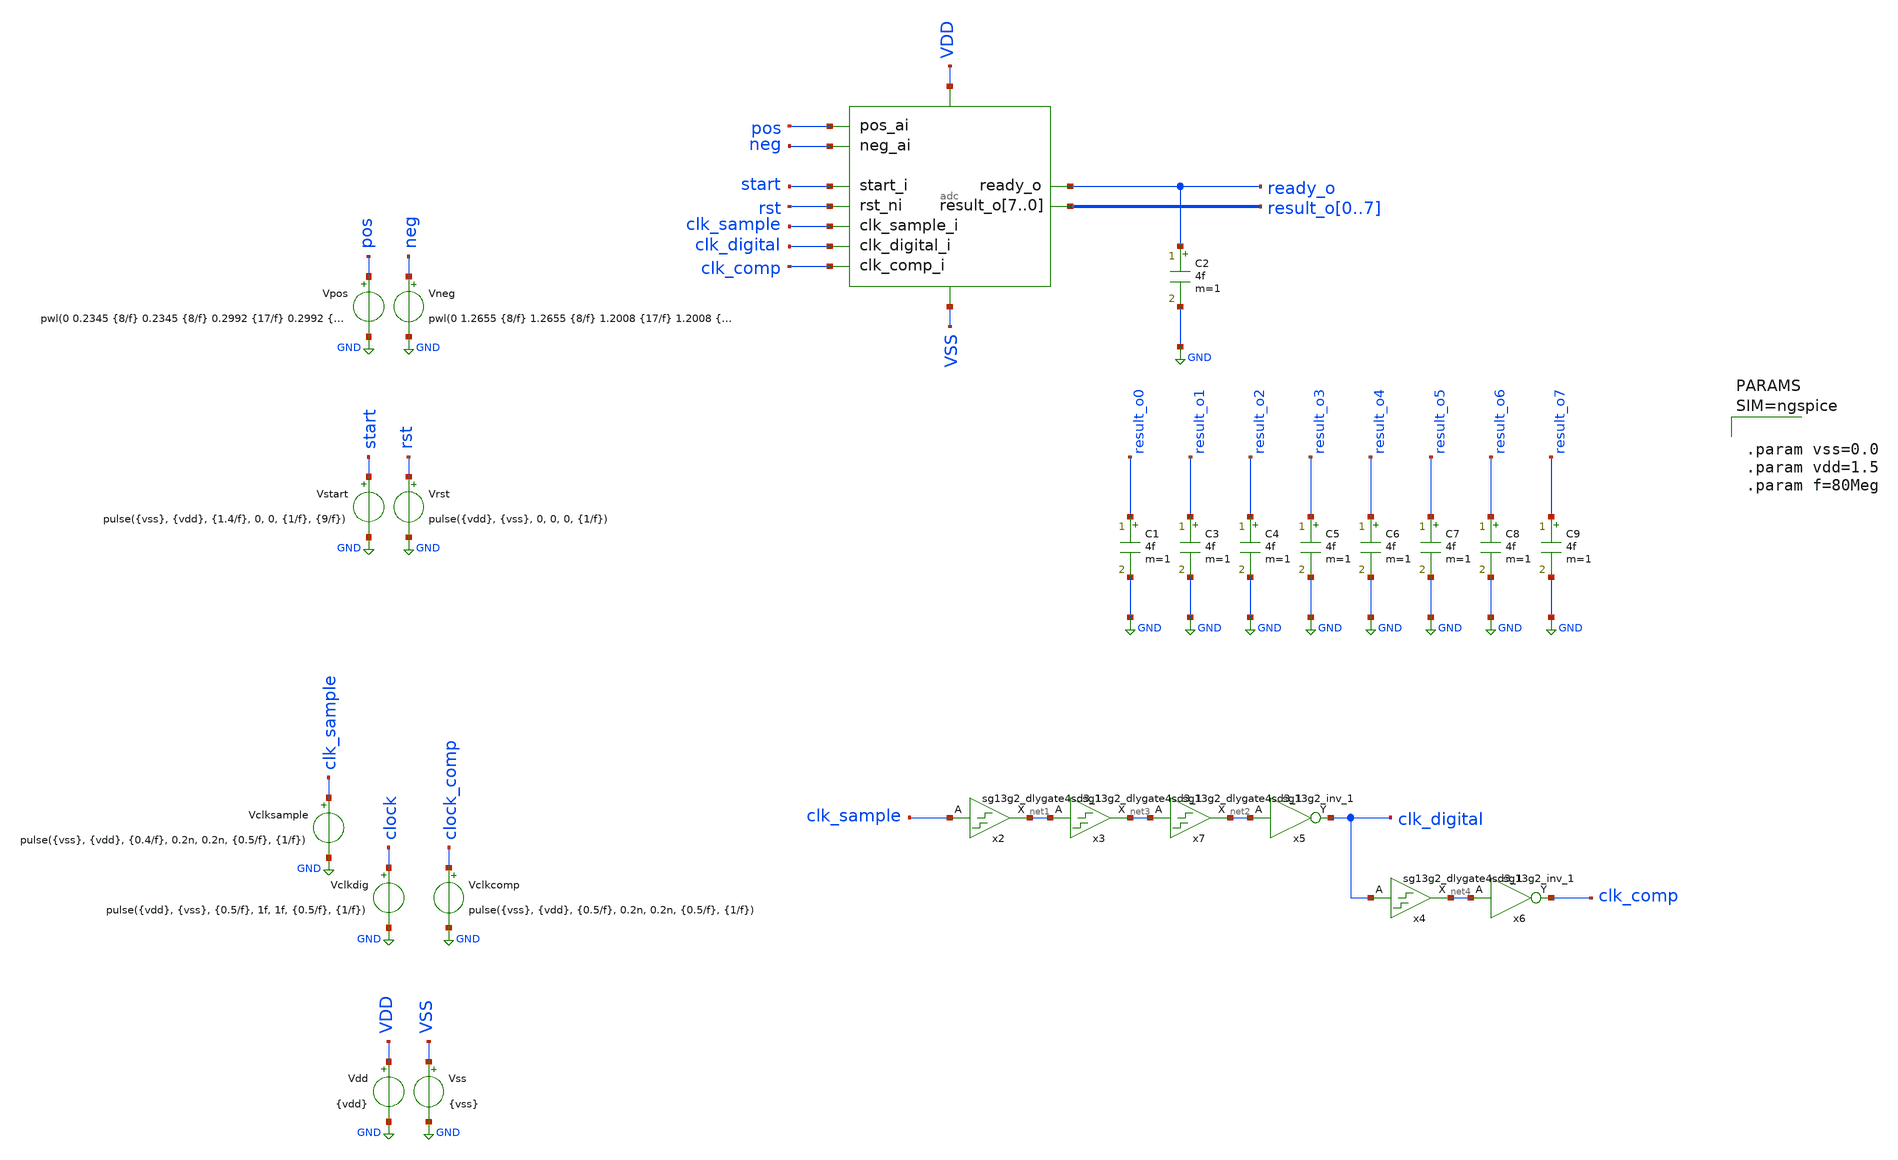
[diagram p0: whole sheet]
** sch_path: project/xschem/adc_tb.sch
* IHP-GmbH/IHP-Open-PDK/ihp-sg13g2/libs.tech/xschem/sg13g2_stdcells/sg13g2_inv_2.sch:
* Copyright 2023 IHP PDK Authors
* Licensed under the Apache License, Version 2.0 (the "License");
**.subckt adc_tb
x1 pos start rst clk_digital result_o0 result_o1 result_o2 result_o3 result_o4 result_o5 result_o6
+ result_o7 ready_o VDD VSS clk_comp neg clk_sample adc
Vclkdig clock GND pulse({vdd}, {vss}, {0.5/f}, 1f, 1f, {0.5/f}, {1/f})
Vrst rst GND pulse({vdd}, {vss}, 0, 0, 0, {1/f})
Vstart start GND pulse({vss}, {vdd}, {1.4/f}, 0, 0, {1/f}, {9/f})
Vpos pos GND pwl(0 0.2345 {8/f} 0.2345 {8/f} 0.2992 {17/f} 0.2992 {17/f} 0.3639 {26/f} 0.3639 {26/f}
+ 0.4286 {35/f} 0.4286 {35/f} 0.4933 {44/f} 0.4933 {44/f} 0.5580 {53/f} 0.5580 {53/f} 0.6227 {62/f} 0.6227
+ {62/f} 0.6875 {71/f} 0.6875 {71/f} 0.7522 {80/f} 0.7522 {80/f} 0.8169 {89/f} 0.8169 {89/f} 0.8816 {98/f}
+ 0.8816 {98/f} 0.9463 {107/f} 0.9463 {107/f} 1.0110 {116/f} 1.0110 {116/f} 1.0757 {125/f} 1.0757 {125/f}
+ 1.1404 {134/f} 1.1404 {134/f} 1.2051 {143/f} 1.2051 {143/f} 1.2698 {152/f} 1.2698)
.save i(vpos)
Vdd VDD GND {vdd}
Vss VSS GND {vss}
C1 result_o0 GND 4f m=1
C2 ready_o GND 4f m=1
C3 result_o1 GND 4f m=1
C4 result_o2 GND 4f m=1
C5 result_o3 GND 4f m=1
Vclkcomp clock_comp GND pulse({vss}, {vdd}, {0.5/f}, 0.2n, 0.2n, {0.5/f}, {1/f})
C6 result_o4 GND 4f m=1
C7 result_o5 GND 4f m=1
C8 result_o6 GND 4f m=1
C9 result_o7 GND 4f m=1
Vneg neg GND pwl(0 1.2655 {8/f} 1.2655 {8/f} 1.2008 {17/f} 1.2008 {17/f} 1.1361 {26/f} 1.1361 {26/f}
+ 1.0714 {35/f} 1.0714 {35/f} 1.0067 {44/f} 1.0067 {44/f} 0.9420 {53/f} 0.9420 {53/f} 0.8773 {62/f} 0.8773
+ {62/f} 0.8125 {71/f} 0.8125 {71/f} 0.7478 {80/f} 0.7478 {80/f} 0.6831 {89/f} 0.6831 {89/f} 0.6184 {98/f}
+ 0.6184 {98/f} 0.5537 {107/f} 0.5537 {107/f} 0.4890 {116/f} 0.4890 {116/f} 0.4243 {125/f} 0.4243 {125/f}
+ 0.3596 {134/f} 0.3596 {134/f} 0.2949 {143/f} 0.2949 {143/f} 0.2302 {152/f} 0.2302)
.save i(vneg)
Vclksample clk_sample GND pulse({vss}, {vdd}, {0.4/f}, 0.2n, 0.2n, {0.5/f}, {1/f})
x2 net1 clk_sample VDD VSS sg13g2_dlygate4sd3_1
x3 net3 net1 VDD VSS sg13g2_dlygate4sd3_1
x5 clk_digital net2 VDD VSS sg13g2_inv_1
x6 clk_comp net4 VDD VSS sg13g2_inv_1
x7 net2 net3 VDD VSS sg13g2_dlygate4sd3_1
x4 net4 clk_digital VDD VSS sg13g2_dlygate4sd3_1
**** begin user architecture code

.lib $::SG13G2_MODELS/cornerMOSlv.lib mos_tt
.lib $::SG13G2_MODELS/cornerCAP.lib cap_typ
.include $::PDK_ROOT/ihp-sg13g2/libs.ref/sg13g2_stdcell/spice/sg13g2_stdcell.spice




*.options method=gear maxord=2
*.options reltol=1e-3 abstol=1e-10 vntol=1e-6 chgtol=1e-14
.options gmin=1e-9 rshunt=1e12

.control
  save all
  tran 1n 2.1u
  * tran 1n 70n
  write adc_tb.raw
.endc






.param vss=0.0
.param vdd=1.5
.param f=80Meg






.model adc_buff_clk adc_bridge(in_low=0.75 in_high=0.75)

.control
pre_set auto_bridge_d_out =  ( ".model auto_bridge_out bidi_bridge(direction=0 out_high=1.5
+ t_rise=0.2n t_fall=0.2n)"    "auto_bridge_out%d [ %s ] [ %s ] null auto_bridge_out" )
pre_set auto_bridge_d_in =  ( ".model auto_bridge_in bidi_bridge(direction=1 in_low=0.5 in_high=1)"
+    "auto_bridge_in%d [ %s ] [ %s ] null auto_bridge_in" )
.endc



**** end user architecture code
**.ends

* expanding   symbol:  adc.sym # of pins=11
** sym_path: project/xschem_gatelevel/adc.sym
** sch_path: project/xschem_gatelevel/adc.sch
.subckt adc pos_ai start_i rst_ni clk_digital_i result_o7 result_o6 result_o5 result_o4 result_o3
+ result_o2 result_o1 result_o0 ready_o VDD VSS clk_comp_i neg_ai clk_sample_i
*.ipin pos_ai
*.ipin VSS
*.ipin VDD
*.ipin clk_comp_i
*.ipin neg_ai
*.ipin clk_sample_i
*.ipin rst_ni
*.ipin clk_digital_i
*.ipin start_i
*.opin ready_o
*.opin result_o7,result_o6,result_o5,result_o4,result_o3,result_o2,result_o1,result_o0
x2 net4 pos neg comp_2 comp_1 VSS VDD net5 comparator
x4 pos neg VSS VDD dac_p0 dac_p1 dac_p2 dac_p3 dac_p4 dac_p5 dac_p6 dac_p0 dac_n0 dac_n1 dac_n2
+ dac_n3 dac_n4 dac_n5 dac_n6 dac_n0 cdac
XM5 comp_p comp_1 VSS VSS sg13_lv_nmos w=1.5u l=0.13u ng=1 m=1 mm_ok=1
XM6 comp_p comp_1 VDD VDD sg13_lv_pmos w=0.15u l=0.13u ng=1 m=1 mm_ok=1
XM7 comp_n comp_2 VSS VSS sg13_lv_nmos w=1.5u l=0.13u ng=1 m=1 mm_ok=1
XM8 comp_n comp_2 VDD VDD sg13_lv_pmos w=0.15u l=0.13u ng=1 m=1 mm_ok=1
x6 sample net1 net2 net1 rst_ni VDD VSS sg13g2_dfrbp_1
x5 net2 clk_sample_i sample_en VDD VSS sg13g2_and2_1
x7 compare clk_comp_i compare_en VDD VSS sg13g2_and2_1
A4 [ clk_digital_i ] [ net3 ] adc_buff_clk
A1 [ net3 comp_n comp_p rst_ni start_i ] [ compare_en dac_n6 dac_n5 dac_n4 dac_n3 dac_n2 dac_n1
+ dac_n0 dac_p6 dac_p5 dac_p4 dac_p3 dac_p2 dac_p1 dac_p0 ready_o result_o7 result_o6 result_o5 result_o4
+ result_o3 result_o2 result_o1 result_o0 sample_en ] adc
.ends


* expanding   symbol:  sg13g2_stdcells/sg13g2_dlygate4sd3_1.sym # of pins=2
** sym_path: sg13g2_stdcells/sg13g2_dlygate4sd3_1.sym
** sch_path: sg13g2_stdcells/sg13g2_dlygate4sd3_1.sch
.subckt sg13g2_dlygate4sd3_1 X A VDD VSS
*.ipin A
*.opin X
*.iopin VDD
*.iopin VSS
XM1 net3 A VSS VSS sg13_lv_nmos w=420.00n l=130.00n ng=1 m=1 mm_ok=1
XM2 net1 net3 VSS VSS sg13_lv_nmos w=420.00n l=500.0n ng=1 m=1 mm_ok=1
XM3 net2 net1 VSS VSS sg13_lv_nmos w=420.00n l=500.0n ng=1 m=1 mm_ok=1
XM4 X net2 VSS VSS sg13_lv_nmos w=740.00n l=130.00n ng=1 m=1 mm_ok=1
XM5 net3 A VDD VDD sg13_lv_pmos w=420.00n l=130.00n ng=1 m=1 mm_ok=1
XM6 net1 net3 VDD VDD sg13_lv_pmos w=1.000u l=500.0n ng=1 m=1 mm_ok=1
XM7 net2 net1 VDD VDD sg13_lv_pmos w=1.000u l=500.0n ng=1 m=1 mm_ok=1
XM8 X net2 VDD VDD sg13_lv_pmos w=1.12u l=130.00n ng=1 m=1 mm_ok=1
.ends


* expanding   symbol:  sg13g2_stdcells/sg13g2_inv_1.sym # of pins=2
** sym_path: sg13g2_stdcells/sg13g2_inv_1.sym
** sch_path: sg13g2_stdcells/sg13g2_inv_1.sch
.subckt sg13g2_inv_1 Y A VDD VSS
*.opin Y
*.ipin A
*.iopin VDD
*.iopin VSS
XM1 Y A VSS VSS sg13_lv_nmos w=740.00n l=130.00n ng=1 m=1 mm_ok=1
XM2 Y A VDD VDD sg13_lv_pmos w=1.12u l=130.00n ng=1 m=1 mm_ok=1
.ends


* expanding   symbol:  ./comparator.sym # of pins=8
** sym_path: designs/comparator_dt/comparator.sym
** sch_path: designs/comparator_dt/comparator.sch
.subckt comparator clk_i pos_ai neg_ai neg_o pos_o VSS VDD clk_ni
*.ipin pos_ai
*.ipin neg_ai
*.ipin VSS
*.ipin VDD
*.opin neg_o
*.opin pos_o
*.ipin clk_i
*.ipin clk_ni
XM12 neg_buf clk_i VDD VDD sg13_lv_pmos w=1.0u l=0.13u ng=1 m=1 mm_ok=1
XM13 pos_buf clk_i VDD VDD sg13_lv_pmos w=1.0u l=0.13u ng=1 m=1 mm_ok=1
XM14 net1 pos_ai neg_buf VSS sg13_lv_nmos w=1.0u l=0.13u ng=1 m=1 mm_ok=1
XM15 net1 neg_ai pos_buf VSS sg13_lv_nmos w=1.0u l=0.13u ng=1 m=1 mm_ok=1
XM16 VSS clk_i net1 VSS sg13_lv_nmos w=1.0u l=0.13u ng=1 m=1 mm_ok=1
XM17 net2 clk_ni VDD VDD sg13_lv_pmos w=2.0u l=0.13u ng=2 m=1 mm_ok=1
XM18 pos_o neg_o net2 VDD sg13_lv_pmos w=2.0u l=0.13u ng=2 m=1 mm_ok=1
XM19 neg_o pos_o net2 VDD sg13_lv_pmos w=2.0u l=0.13u ng=2 m=1 mm_ok=1
XM20 VSS neg_buf pos_o VSS sg13_lv_nmos w=1.0u l=0.13u ng=1 m=1 mm_ok=1
XM21 VSS neg_o pos_o VSS sg13_lv_nmos w=1.0u l=0.13u ng=1 m=1 mm_ok=1
XM22 VSS pos_o neg_o VSS sg13_lv_nmos w=1.0u l=0.13u ng=1 m=1 mm_ok=1
XM23 VSS pos_buf neg_o VSS sg13_lv_nmos w=1.0u l=0.13u ng=1 m=1 mm_ok=1
XC1 neg_buf VSS cap_cmim w=1.41e-5 l=1.41e-5 m=1 mm_ok=1
XC2 pos_buf VSS cap_cmim w=1.41e-5 l=1.41e-5 m=1 mm_ok=1
.ends


* expanding   symbol:  ./cdac.sym # of pins=6
** sym_path: designs/cdac_diff/cdac.sym
** sch_path: designs/cdac_diff/cdac.sch
.subckt cdac pos_ai neg_ai VSS VDD pos_ctrl_i0 pos_ctrl_i1 pos_ctrl_i2 pos_ctrl_i3 pos_ctrl_i4
+ pos_ctrl_i5 pos_ctrl_i6 pos_ctrl_i7 neg_ctrl_i0 neg_ctrl_i1 neg_ctrl_i2 neg_ctrl_i3 neg_ctrl_i4 neg_ctrl_i5
+ neg_ctrl_i6 neg_ctrl_i7
*.ipin pos_ai
*.ipin VSS
*.ipin VDD
*.ipin neg_ai
*.ipin
*+ pos_ctrl_i0,pos_ctrl_i1,pos_ctrl_i2,pos_ctrl_i3,pos_ctrl_i4,pos_ctrl_i5,pos_ctrl_i6,pos_ctrl_i7
*.ipin
*+ neg_ctrl_i0,neg_ctrl_i1,neg_ctrl_i2,neg_ctrl_i3,neg_ctrl_i4,neg_ctrl_i5,neg_ctrl_i6,neg_ctrl_i7
x1 net1 pos_ctrl_i0 VDD VSS sg13g2_inv_2
x2 net2 pos_ctrl_i1 VDD VSS sg13g2_inv_2
x3 net3 pos_ctrl_i2 VDD VSS sg13g2_inv_2
x4 net4 pos_ctrl_i3 VDD VSS sg13g2_inv_2
x5 net5 pos_ctrl_i4 VDD VSS sg13g2_inv_2
x6 net6 pos_ctrl_i5 VDD VSS sg13g2_inv_2
x7 net7 pos_ctrl_i6 VDD VSS sg13g2_inv_2
x8 net8 pos_ctrl_i7 VDD VSS sg13g2_inv_2
XC1 pos_ai net8 cap_cmim w=2.5292e-6 l=2.5292e-6 m=1 mm_ok=1
XC2 pos_ai net7 cap_cmim w=2.5292e-6 l=2.5292e-6 m=2 mm_ok=1
XC3 pos_ai net6 cap_cmim w=2.5292e-6 l=2.5292e-6 m=4 mm_ok=1
XC4 pos_ai net5 cap_cmim w=2.5292e-6 l=2.5292e-6 m=8 mm_ok=1
XC9 pos_ai VSS cap_cmim w=2.5292e-6 l=2.5292e-6 m=1 mm_ok=1
x9 net9 neg_ctrl_i0 VDD VSS sg13g2_inv_2
x10 net10 neg_ctrl_i1 VDD VSS sg13g2_inv_2
x11 net11 neg_ctrl_i2 VDD VSS sg13g2_inv_2
x12 net12 neg_ctrl_i3 VDD VSS sg13g2_inv_2
x13 net13 neg_ctrl_i4 VDD VSS sg13g2_inv_2
x14 net14 neg_ctrl_i5 VDD VSS sg13g2_inv_2
x15 net15 neg_ctrl_i6 VDD VSS sg13g2_inv_2
x16 net16 neg_ctrl_i7 VDD VSS sg13g2_inv_2
XC10 neg_ai net16 cap_cmim w=2.5292e-6 l=2.5292e-6 m=1 mm_ok=1
XC11 neg_ai net15 cap_cmim w=2.5292e-6 l=2.5292e-6 m=2 mm_ok=1
XC12 neg_ai net14 cap_cmim w=2.5292e-6 l=2.5292e-6 m=4 mm_ok=1
XC13 neg_ai net13 cap_cmim w=2.5292e-6 l=2.5292e-6 m=8 mm_ok=1
XC18 neg_ai VSS cap_cmim w=2.5292e-6 l=2.5292e-6 m=1 mm_ok=1
XC8 pos_ai net1 cap_cmim w=2.5292e-6 l=2.5292e-6 m=64 mm_ok=1
XC17 neg_ai net9 cap_cmim w=2.5292e-6 l=2.5292e-6 m=64 mm_ok=1
XC19 neg_ai net18 cap_cmim w=2.5292e-6 l=2.5292e-6 m=64 mm_ok=1
XC20 pos_ai net17 cap_cmim w=2.5292e-6 l=2.5292e-6 m=64 mm_ok=1
XC7 neg_ai net10 cap_cmim w=2.5292e-6 l=2.5292e-6 m=32 mm_ok=1
XC16 pos_ai net2 cap_cmim w=2.5292e-6 l=2.5292e-6 m=32 mm_ok=1
XC21 pos_ai net19 cap_cmim w=2.5292e-6 l=2.5292e-6 m=32 mm_ok=1
XC22 neg_ai net20 cap_cmim w=2.5292e-6 l=2.5292e-6 m=32 mm_ok=1
XC23 neg_ai net22 cap_cmim w=2.5292e-6 l=2.5292e-6 m=16 mm_ok=1
XC24 pos_ai net21 cap_cmim w=2.5292e-6 l=2.5292e-6 m=16 mm_ok=1
XC6 neg_ai net11 cap_cmim w=2.5292e-6 l=2.5292e-6 m=16 mm_ok=1
XC15 pos_ai net3 cap_cmim w=2.5292e-6 l=2.5292e-6 m=16 mm_ok=1
XC25 neg_ai net24 cap_cmim w=2.5292e-6 l=2.5292e-6 m=8 mm_ok=1
XC26 pos_ai net23 cap_cmim w=2.5292e-6 l=2.5292e-6 m=8 mm_ok=1
XC5 pos_ai net4 cap_cmim w=2.5292e-6 l=2.5292e-6 m=8 mm_ok=1
XC14 neg_ai net12 cap_cmim w=2.5292e-6 l=2.5292e-6 m=8 mm_ok=1
* noconn VDD
x17 net17 neg_ctrl_i0 VDD VSS sg13g2_buf_2
x21 net18 pos_ctrl_i0 VDD VSS sg13g2_buf_2
x18 net19 neg_ctrl_i1 VDD VSS sg13g2_buf_2
x19 net20 pos_ctrl_i1 VDD VSS sg13g2_buf_2
x20 net21 neg_ctrl_i2 VDD VSS sg13g2_buf_2
x22 net22 pos_ctrl_i2 VDD VSS sg13g2_buf_2
x23 net23 neg_ctrl_i3 VDD VSS sg13g2_buf_2
x24 net24 pos_ctrl_i3 VDD VSS sg13g2_buf_2
.ends


* expanding   symbol:  sg13g2_stdcells/sg13g2_dfrbp_1.sym # of pins=5
** sym_path: sg13g2_stdcells/sg13g2_dfrbp_1.sym
** sch_path: sg13g2_stdcells/sg13g2_dfrbp_1.sch
.subckt sg13g2_dfrbp_1 Q Q_N CLK D RESET_B VDD VSS
*.ipin D
*.ipin RESET_B
*.ipin CLK
*.opin Q
*.opin Q_N
*.iopin VDD
*.iopin VSS
XM1 Db D net10 VSS sg13_lv_nmos w=420.00n l=130.00n ng=1 m=1 mm_ok=1
XM2 net10 RESET_B VSS VSS sg13_lv_nmos w=420.00n l=130.00n ng=1 m=1 mm_ok=1
XM3 net1 clkneg net9 VSS sg13_lv_nmos w=420.00n l=130.00n ng=1 m=1 mm_ok=1
XM4 net9 net1 VSS VSS sg13_lv_nmos w=420.00n l=130.00n ng=1 m=1 mm_ok=1
XM5 net1 net1 net5 VSS sg13_lv_nmos w=420.00n l=130.00n ng=1 m=1 mm_ok=1
XM6 net5 RESET_B VSS VSS sg13_lv_nmos w=420.00n l=130.00n ng=1 m=1 mm_ok=1
XM7 Q_N net1 VSS VSS sg13_lv_nmos w=740.00n l=130.00n ng=1 m=1 mm_ok=1
XM8 net2 net1 VSS VSS sg13_lv_nmos w=740.00n l=130.00n ng=1 m=1 mm_ok=1
XM9 Q net2 VSS VSS sg13_lv_nmos w=740.00n l=130.00n ng=1 m=1 mm_ok=1
XM10 clkneg CLK VSS VSS sg13_lv_nmos w=740.00n l=130.00n ng=1 m=1 mm_ok=1
XM11 clkpos clkneg VSS VSS sg13_lv_nmos w=740.00n l=130.00n ng=1 m=1 mm_ok=1
XM12 Db clkneg net3 VSS sg13_lv_nmos w=420.00n l=130.00n ng=1 m=1 mm_ok=1
XM13 net3 clkpos net8 VSS sg13_lv_nmos w=420.00n l=130.00n ng=1 m=1 mm_ok=1
XM14 net8 net3 net4 VSS sg13_lv_nmos w=420.00n l=130.00n ng=1 m=1 mm_ok=1
XM15 net4 RESET_B VSS VSS sg13_lv_nmos w=420.00n l=130.00n ng=1 m=1 mm_ok=1
XM16 net3 net3 VSS VSS sg13_lv_nmos w=740.00n l=130.00n ng=1 m=1 mm_ok=1
XM17 net3 clkpos net1 VSS sg13_lv_nmos w=740.00n l=130.00n ng=1 m=1 mm_ok=1
XM18 Db RESET_B VDD VDD sg13_lv_pmos w=420.00n l=130.00n ng=1 m=1 mm_ok=1
XM19 Db D VDD VDD sg13_lv_pmos w=420.00n l=130.00n ng=1 m=1 mm_ok=1
XM20 net7 net1 VDD VDD sg13_lv_pmos w=420.00n l=130.00n ng=1 m=1 mm_ok=1
XM21 net1 clkpos net7 VDD sg13_lv_pmos w=420.00n l=130.00n ng=1 m=1 mm_ok=1
XM22 net1 net1 VDD VDD sg13_lv_pmos w=420.00n l=130.00n ng=1 m=1 mm_ok=1
XM23 net1 RESET_B VDD VDD sg13_lv_pmos w=420.00n l=130.00n ng=1 m=1 mm_ok=1
XM24 Q_N net1 VDD VDD sg13_lv_pmos w=1.12u l=130.00n ng=1 m=1 mm_ok=1
XM25 net2 net1 VDD VDD sg13_lv_pmos w=1.12u l=130.00n ng=1 m=1 mm_ok=1
XM26 Q net2 VDD VDD sg13_lv_pmos w=1.12u l=130.00n ng=1 m=1 mm_ok=1
XM27 clkneg CLK VDD VDD sg13_lv_pmos w=1.12u l=130.00n ng=1 m=1 mm_ok=1
XM28 clkpos clkneg VDD VDD sg13_lv_pmos w=1.12u l=130.00n ng=1 m=1 mm_ok=1
XM29 Db clkpos net3 VDD sg13_lv_pmos w=420.00n l=130.00n ng=1 m=1 mm_ok=1
XM30 net6 net3 VDD VDD sg13_lv_pmos w=420.00n l=130.00n ng=1 m=1 mm_ok=1
XM31 net3 clkneg net6 VDD sg13_lv_pmos w=420.00n l=130.00n ng=1 m=1 mm_ok=1
XM32 net3 RESET_B VDD VDD sg13_lv_pmos w=420.00n l=130.00n ng=1 m=1 mm_ok=1
XM33 net3 net3 VDD VDD sg13_lv_pmos w=1.000u l=130.00n ng=1 m=1 mm_ok=1
XM34 net3 clkneg net1 VDD sg13_lv_pmos w=1.000u l=130.00n ng=1 m=1 mm_ok=1
.ends


* expanding   symbol:  sg13g2_stdcells/sg13g2_and2_1.sym # of pins=3
** sym_path: sg13g2_stdcells/sg13g2_and2_1.sym
** sch_path: sg13g2_stdcells/sg13g2_and2_1.sch
.subckt sg13g2_and2_1 X A B VDD VSS
*.ipin A
*.ipin B
*.opin X
*.iopin VDD
*.iopin VSS
XM1 net1 A net2 VSS sg13_lv_nmos w=640.00n l=130.00n ng=1 m=1 mm_ok=1
XM2 net2 B VSS VSS sg13_lv_nmos w=640.00n l=130.00n ng=1 m=1 mm_ok=1
XM3 X net1 VSS VSS sg13_lv_nmos w=740.00n l=130.00n ng=1 m=1 mm_ok=1
XM4 net1 B VDD VDD sg13_lv_pmos w=840.00n l=130.00n ng=1 m=1 mm_ok=1
XM5 net1 A VDD VDD sg13_lv_pmos w=840.00n l=130.00n ng=1 m=1 mm_ok=1
XM6 X net1 VDD VDD sg13_lv_pmos w=1.12u l=130.00n ng=1 m=1 mm_ok=1
.ends


* expanding   symbol:  sg13g2_stdcells/sg13g2_inv_2.sym # of pins=2
** sym_path: sg13g2_stdcells/sg13g2_inv_2.sym
** sch_path: sg13g2_stdcells/sg13g2_inv_2.sch
.subckt sg13g2_inv_2 Y A VDD VSS
*.opin Y
*.ipin A
*.iopin VDD
*.iopin VSS
XM1 Y A VSS VSS sg13_lv_nmos w=1.48u l=130.00n ng=2 m=1 mm_ok=1
XM2 Y A VDD VDD sg13_lv_pmos w=2.24u l=130.00n ng=2 m=1 mm_ok=1
.ends


* expanding   symbol:  sg13g2_stdcells/sg13g2_buf_2.sym # of pins=2
** sym_path: sg13g2_stdcells/sg13g2_buf_2.sym
** sch_path: sg13g2_stdcells/sg13g2_buf_2.sch
.subckt sg13g2_buf_2 X A VDD VSS
*.ipin A
*.opin X
*.iopin VDD
*.iopin VSS
XM1 net1 A VSS VSS sg13_lv_nmos w=640.00n l=130.00n ng=1 m=1 mm_ok=1
XM2 X net1 VSS VSS sg13_lv_nmos w=1.48u l=130.00n ng=2 m=1 mm_ok=1
XM3 net1 A VDD VDD sg13_lv_pmos w=1.000u l=130.00n ng=1 m=1 mm_ok=1
XM4 X net1 VDD VDD sg13_lv_pmos w=2.24u l=130.00n ng=2 m=1 mm_ok=1
.ends

.GLOBAL GND
**** begin user architecture code
.model adc d_cosim simulation="ivlng" sim_args=["adc"]
**** end user architecture code
.end
